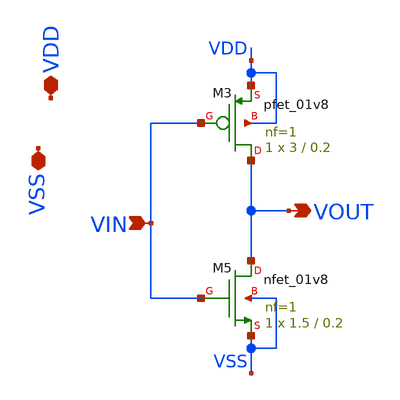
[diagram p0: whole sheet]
** sch_path: Xschem/PLL_TOP_Schematics/inverter_1.sch
**.subckt inverter_1 VOUT VSS VDD VIN
*.opin VOUT
*.iopin VSS
*.iopin VDD
*.ipin VIN
XM3 VOUT VIN VDD VDD sky130_fd_pr__pfet_01v8 L=0.2 W=3 nf=1 ad='int((nf+1)/2) * W/nf * 0.29' as='int((nf+2)/2) * W/nf * 0.29'
+ pd='2*int((nf+1)/2) * (W/nf + 0.29)' ps='2*int((nf+2)/2) * (W/nf + 0.29)' nrd='0.29 / W' nrs='0.29 / W'
+ sa=0 sb=0 sd=0 mult=1 m=1
XM5 VOUT VIN VSS VSS sky130_fd_pr__nfet_01v8 L=0.2 W=1.5 nf=1 ad='int((nf+1)/2) * W/nf * 0.29' as='int((nf+2)/2) * W/nf * 0.29'
+ pd='2*int((nf+1)/2) * (W/nf + 0.29)' ps='2*int((nf+2)/2) * (W/nf + 0.29)' nrd='0.29 / W' nrs='0.29 / W'
+ sa=0 sb=0 sd=0 mult=1 m=1
**.ends
.end
